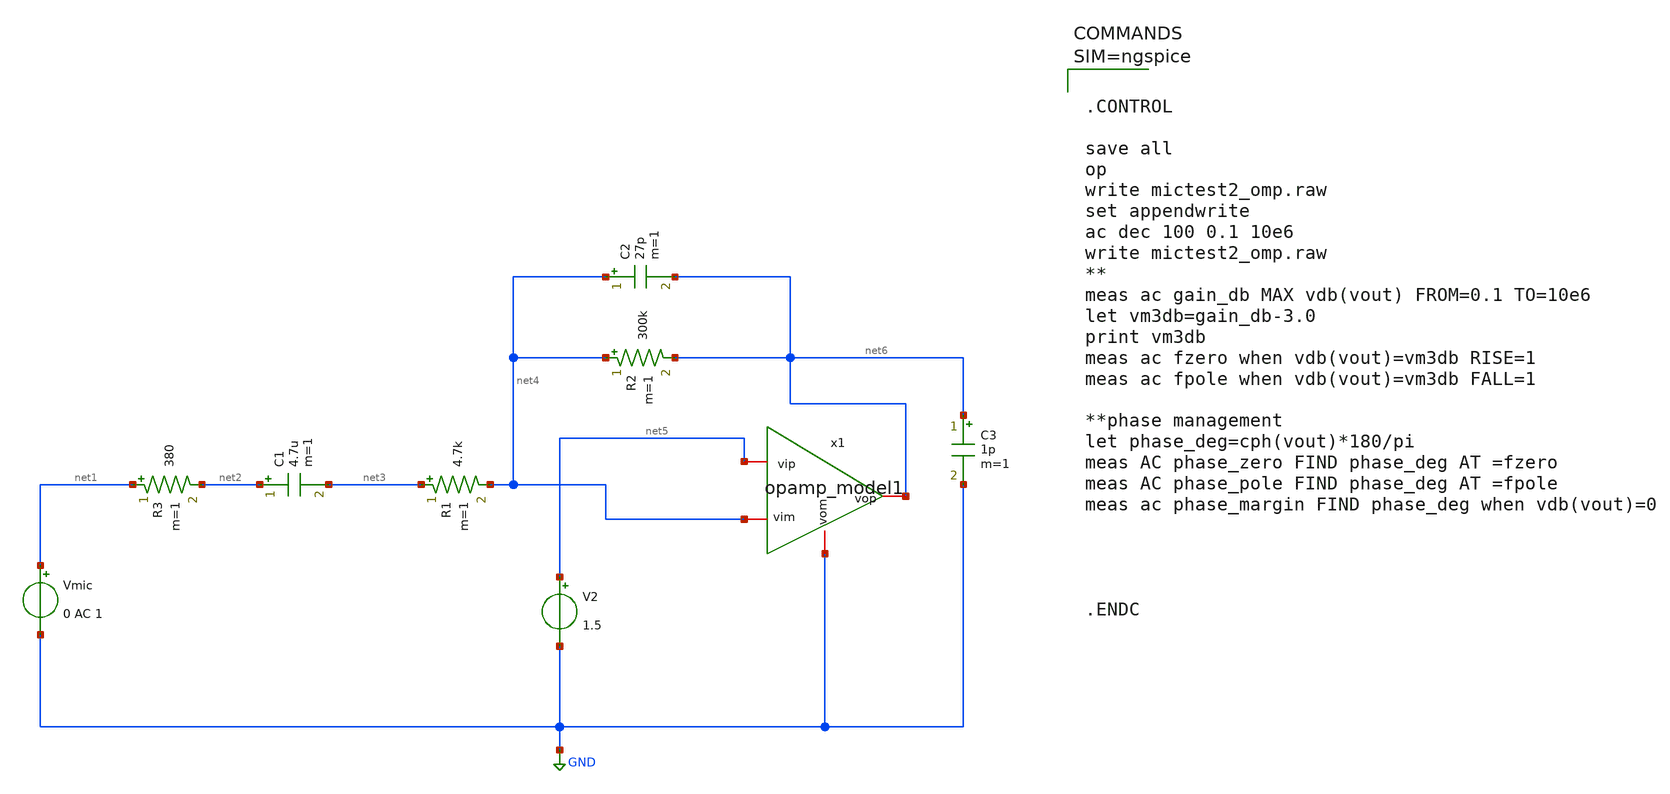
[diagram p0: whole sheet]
** sch_path: work/xschem/mictest2_omp.sch
**.subckt mictest2_omp
R1 net3 net4 4.7k m=1
C1 net2 net3 4.7u m=1
V2 net5 GND 1.5
R2 net4 net6 300k m=1
C2 net4 net6 27p m=1
C3 net6 GND 1p m=1
R3 net1 net2 380 m=1
Vmic net1 GND 0 AC 1
x1 net6 net5 net4 GND opamp_model1
**** begin user architecture code



.CONTROL

save all
op
write mictest2_omp.raw
set appendwrite
ac dec 100 0.1 10e6
write mictest2_omp.raw
**
meas ac gain_db MAX vdb(vout) FROM=0.1 TO=10e6
let vm3db=gain_db-3.0
print vm3db
meas ac fzero when vdb(vout)=vm3db RISE=1
meas ac fpole when vdb(vout)=vm3db FALL=1

**phase management
let phase_deg=cph(vout)*180/pi
meas AC phase_zero FIND phase_deg AT =fzero
meas AC phase_pole FIND phase_deg AT =fpole
meas ac phase_margin FIND phase_deg when vdb(vout)=0




.ENDC



**** end user architecture code
**.ends

* expanding   symbol:  opamp_model1.sym # of pins=4
** sym_path: work/xschem/opamp_model1.sym
** sch_path: work/xschem/opamp_model1.sch
.subckt opamp_model1 vop vip vim vom
*.iopin vop
*.iopin vom
*.iopin vim
*.iopin vip
E1 vop vom vip vim 1000
.ends

.GLOBAL GND
.end
